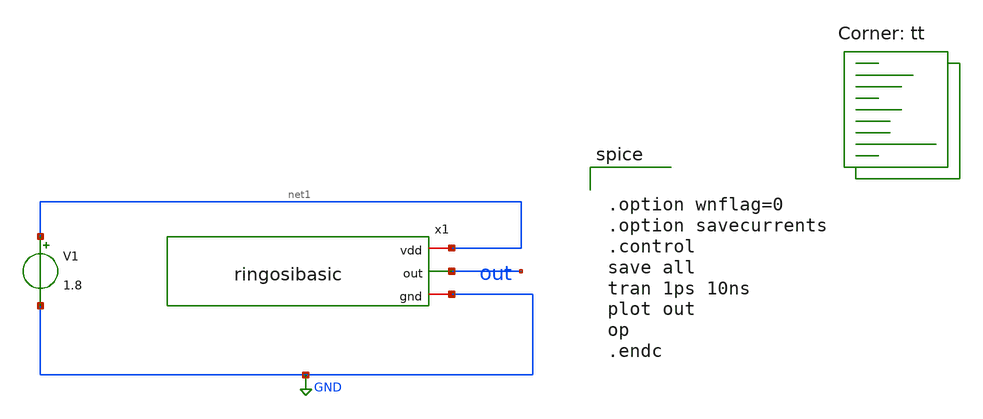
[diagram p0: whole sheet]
** sch_path: oscillator/oscillator/ringosibasictb.sch
**.subckt ringosibasictb
x1 net1 out GND ringosibasic
V1 net1 GND 1.8
**** begin user architecture code
.lib $::SKYWATER_MODELS/sky130.lib.spice tt


.option wnflag=0
.option savecurrents
.control
save all
tran 1ps 10ns
plot out
op
.endc


**** end user architecture code
**.ends

* expanding   symbol:  ringosibasic.sym # of pins=3
** sym_path: oscillator/oscillator/ringosibasic.sym
** sch_path: oscillator/oscillator/ringosibasic.sch
.subckt ringosibasic vdd out gnd
*.iopin vdd
*.iopin gnd
*.opin out
x1 vdd out net2 gnd terbaru
x2 vdd net2 net1 gnd terbaru
x3 vdd net1 out gnd terbaru
.ends


* expanding   symbol:  terbaru.sym # of pins=4
** sym_path: oscillator/oscillator/terbaru.sym
** sch_path: oscillator/oscillator/terbaru.sch
.subckt terbaru vdd in out gnd
*.ipin in
*.ipin gnd
*.ipin vdd
*.opin out
XM1 out in gnd gnd sky130_fd_pr__nfet_01v8 L=0.15 W=1 nf=1 ad='int((nf+1)/2) * W/nf * 0.29' as='int((nf+2)/2) * W/nf * 0.29'
+ pd='2*int((nf+1)/2) * (W/nf + 0.29)' ps='2*int((nf+2)/2) * (W/nf + 0.29)' nrd='0.29 / W' nrs='0.29 / W'
+ sa=0 sb=0 sd=0 mult=1 m=1
XM2 out in vdd vdd sky130_fd_pr__pfet_01v8 L=0.15 W=1 nf=1 ad='int((nf+1)/2) * W/nf * 0.29' as='int((nf+2)/2) * W/nf * 0.29'
+ pd='2*int((nf+1)/2) * (W/nf + 0.29)' ps='2*int((nf+2)/2) * (W/nf + 0.29)' nrd='0.29 / W' nrs='0.29 / W'
+ sa=0 sb=0 sd=0 mult=1 m=1
.ends

.GLOBAL GND
.end
